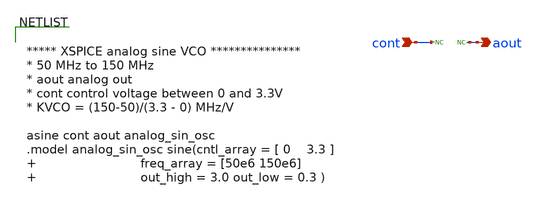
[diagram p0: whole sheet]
** sch_path: designs/libs/model_pll/vco_model.sch
**.subckt vco_model cont aout
*.ipin cont
*.opin aout
* noconn aout
* noconn cont
**** begin user architecture code


***** XSPICE analog sine VCO ***************
* 50 MHz to 150 MHz
* aout analog out
* cont control voltage between 0 and 3.3V
* KVCO = (150-50)/(3.3 - 0) MHz/V

asine cont aout analog_sin_osc
.model analog_sin_osc sine(cntl_array = [ 0    3.3 ]                           freq_array = [50e6
+ 150e6]                           out_high = 3.0 out_low = 0.3 )



**** end user architecture code
**.ends
.end
